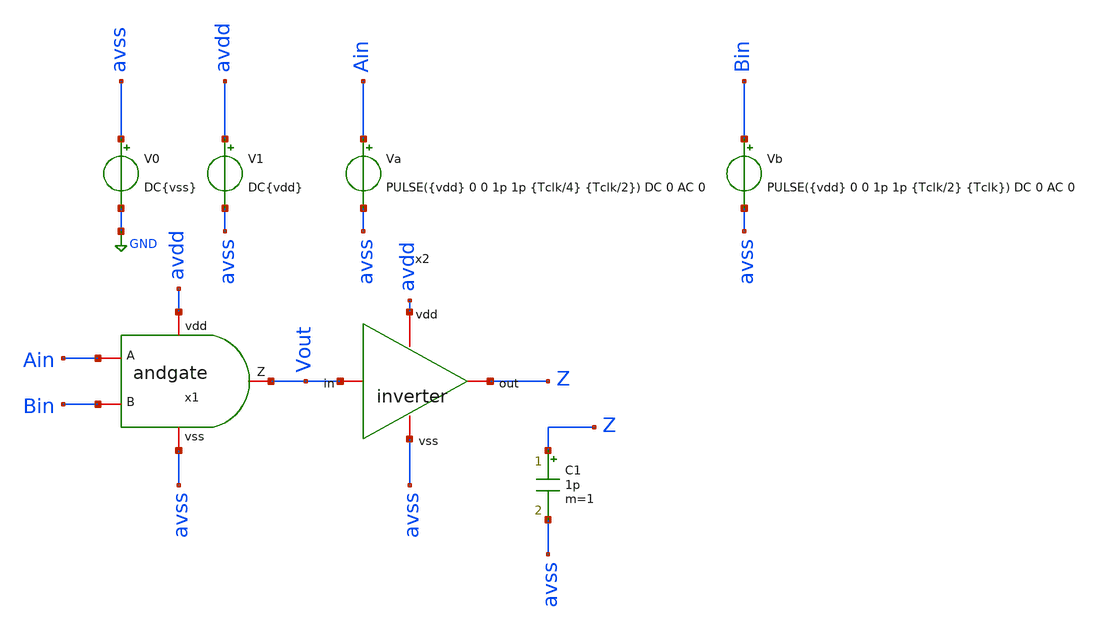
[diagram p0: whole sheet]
** sch_path: tstbnch/andtstbnch.sch
**.subckt andtstbnch
C1 Z avss 1p m=1
V1 avdd avss DC{vdd}
Va Ain avss PULSE({vdd} 0 0 1p 1p {Tclk/4} {Tclk/2}) DC 0 AC 0
V0 avss GND DC{vss}
Vb Bin avss PULSE({vdd} 0 0 1p 1p {Tclk/2} {Tclk}) DC 0 AC 0
x1 avdd Ain Bin Vout avss andgate
x2 avdd Vout Z avss inverter
**** begin user architecture code


* Circuit Parameters
.param vdd = 1.8
.param vss = 0.0
.param Tclk = 20n
.options TEMP = 65.0
* Include Models
.lib /foss/pdks/sky130A/libs.tech/ngspice/sky130.lib.spice TT
* OP Parameters & Singals to save
.save all
*Simulations
.control
tran 0.01u 100n
setplot tran1
plot v(Ain) v(Bin)+2 v(vout)+4
reset
dc Va 0 1.8 0.01
dc Vb 0 1.8 0.01
setplot dc
plot vin vout ylabel vout xlabel vin
set filetype = ascii
write dcsweep.raw
.endc
.end


**** end user architecture code
**.ends

* expanding   symbol:  /foss/designs/sch/andgate.sym # of pins=5
** sym_path: sch/andgate.sym
** sch_path: sch/andgate.sch
.subckt andgate vdd A B Z vss
*.iopin vdd
*.iopin Z
*.iopin A
*.iopin B
*.iopin vss
XM0 net1 A vdd vdd sky130_fd_pr__pfet_01v8 L=0.15 W=1.5 nf=1 ad='int((nf+1)/2) * W/nf * 0.29' as='int((nf+2)/2) * W/nf * 0.29'
+ pd='2*int((nf+1)/2) * (W/nf + 0.29)' ps='2*int((nf+2)/2) * (W/nf + 0.29)' nrd='0.29 / W' nrs='0.29 / W'
+ sa=0 sb=0 sd=0 mult=1 m=1
XM2 net1 A net2 vss sky130_fd_pr__nfet_01v8 L=0.15 W=1.5 nf=1 ad='int((nf+1)/2) * W/nf * 0.29' as='int((nf+2)/2) * W/nf * 0.29'
+ pd='2*int((nf+1)/2) * (W/nf + 0.29)' ps='2*int((nf+2)/2) * (W/nf + 0.29)' nrd='0.29 / W' nrs='0.29 / W'
+ sa=0 sb=0 sd=0 mult=1 m=1
XM3 net2 B vss vss sky130_fd_pr__nfet_01v8 L=0.15 W=1.5 nf=1 ad='int((nf+1)/2) * W/nf * 0.29' as='int((nf+2)/2) * W/nf * 0.29'
+ pd='2*int((nf+1)/2) * (W/nf + 0.29)' ps='2*int((nf+2)/2) * (W/nf + 0.29)' nrd='0.29 / W' nrs='0.29 / W'
+ sa=0 sb=0 sd=0 mult=1 m=1
XM4 Z net1 vdd vdd sky130_fd_pr__pfet_01v8 L=0.15 W=1.5 nf=1 ad='int((nf+1)/2) * W/nf * 0.29' as='int((nf+2)/2) * W/nf * 0.29'
+ pd='2*int((nf+1)/2) * (W/nf + 0.29)' ps='2*int((nf+2)/2) * (W/nf + 0.29)' nrd='0.29 / W' nrs='0.29 / W'
+ sa=0 sb=0 sd=0 mult=1 m=1
XM5 Z net1 vss vss sky130_fd_pr__nfet_01v8 L=0.15 W=0.75 nf=1 ad='int((nf+1)/2) * W/nf * 0.29' as='int((nf+2)/2) * W/nf * 0.29'
+ pd='2*int((nf+1)/2) * (W/nf + 0.29)' ps='2*int((nf+2)/2) * (W/nf + 0.29)' nrd='0.29 / W' nrs='0.29 / W'
+ sa=0 sb=0 sd=0 mult=1 m=1
XM1 net1 B vdd vdd sky130_fd_pr__pfet_01v8 L=0.15 W=1.5 nf=1 ad='int((nf+1)/2) * W/nf * 0.29' as='int((nf+2)/2) * W/nf * 0.29'
+ pd='2*int((nf+1)/2) * (W/nf + 0.29)' ps='2*int((nf+2)/2) * (W/nf + 0.29)' nrd='0.29 / W' nrs='0.29 / W'
+ sa=0 sb=0 sd=0 mult=1 m=1
.ends


* expanding   symbol:  /foss/designs/sch/inverter.sym # of pins=4
** sym_path: sch/inverter.sym
** sch_path: sch/inverter.sch
.subckt inverter vdd in out vss
*.iopin out
*.iopin vdd
*.iopin vss
*.iopin in
XM1 out in vss vss sky130_fd_pr__nfet_01v8 L=0.15 W=0.45 nf=1 ad='int((nf+1)/2) * W/nf * 0.29' as='int((nf+2)/2) * W/nf * 0.29'
+ pd='2*int((nf+1)/2) * (W/nf + 0.29)' ps='2*int((nf+2)/2) * (W/nf + 0.29)' nrd='0.29 / W' nrs='0.29 / W'
+ sa=0 sb=0 sd=0 mult=1 m=1
XM2 out in vdd vdd sky130_fd_pr__pfet_01v8 L=0.15 W=0.45 nf=1 ad='int((nf+1)/2) * W/nf * 0.29' as='int((nf+2)/2) * W/nf * 0.29'
+ pd='2*int((nf+1)/2) * (W/nf + 0.29)' ps='2*int((nf+2)/2) * (W/nf + 0.29)' nrd='0.29 / W' nrs='0.29 / W'
+ sa=0 sb=0 sd=0 mult=1 m=1
.ends

.GLOBAL GND
.end
